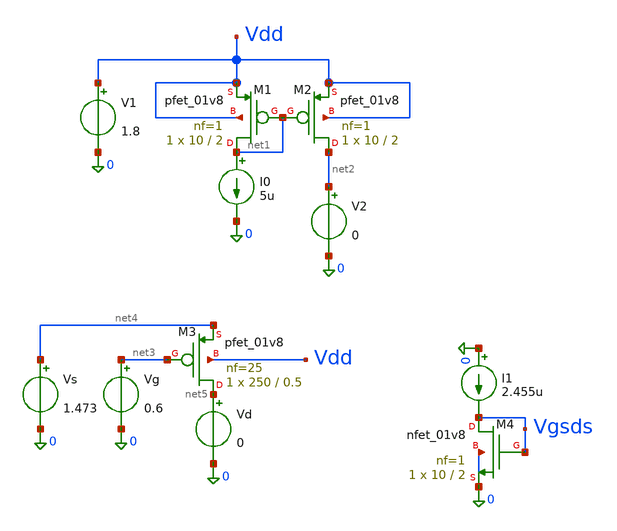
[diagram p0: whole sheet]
** sch_path: stage1/testbenches/stack_headroom_characterization.sch
**.subckt stack_headroom_characterization
I0 net1 0 5u
XM1 net1 net1 Vdd Vdd sky130_fd_pr__pfet_01v8 L=2 W=10 nf=1 ad='int((1 + 1)/2) * 10 / 1 * 0.29' as='int((1 + 2)/2) * 10 / 1 * 0.29'
+ pd='2*int((1 + 1)/2) * (10 / 1 + 0.29)' ps='2*int((1 + 2)/2) * (10 / 1 + 0.29)' nrd='0.29 / 10 ' nrs='0.29 / 10 '
+ sa=0 sb=0 sd=0 mult=1 m=1
XM2 net2 net1 Vdd Vdd sky130_fd_pr__pfet_01v8 L=2 W=10 nf=1 ad='int((1 + 1)/2) * 10 / 1 * 0.29' as='int((1 + 2)/2) * 10 / 1 * 0.29'
+ pd='2*int((1 + 1)/2) * (10 / 1 + 0.29)' ps='2*int((1 + 2)/2) * (10 / 1 + 0.29)' nrd='0.29 / 10 ' nrs='0.29 / 10 '
+ sa=0 sb=0 sd=0 mult=1 m=1
V1 Vdd 0 1.8
V2 net2 0 0
XM3 net5 net3 net4 Vdd sky130_fd_pr__pfet_01v8 L=0.5 W=250 nf=25 ad='int((25 + 1)/2) * 250 / 25 * 0.29'
+ as='int((25 + 2)/2) * 250 / 25 * 0.29' pd='2*int((25 + 1)/2) * (250 / 25 + 0.29)' ps='2*int((25 + 2)/2) * (250 / 25 + 0.29)'
+ nrd='0.29 / 250 ' nrs='0.29 / 250 ' sa=0 sb=0 sd=0 mult=1 m=1
Vg net3 0 0.6
Vd net5 0 0
Vs net4 0 1.473
XM4 Vgsds Vgsds 0 0 sky130_fd_pr__nfet_01v8 L=2 W=10 nf=1 ad='int((1 + 1)/2) * 10 / 1 * 0.29' as='int((1 + 2)/2) * 10 / 1 * 0.29'
+ pd='2*int((1 + 1)/2) * (10 / 1 + 0.29)' ps='2*int((1 + 2)/2) * (10 / 1 + 0.29)' nrd='0.29 / 10 ' nrs='0.29 / 10 '
+ sa=0 sb=0 sd=0 mult=1 m=1
I1 0 Vgsds 2.455u
**** begin user architecture code

** opencircuitdesign pdks install
.lib $::SKYWATER_MODELS/sky130.lib.spice tt


.options savecurrents

.control
	save all
	#dc V2 0 1.5 0.01
	#let Vsd = v(Vdd)-v(net2)
	#let Id = V2#branch
	#let mirror_accuracy = Id/5u
	#plot Id vs Vsd
	#plot mirror_accuracy vs Vsd

	#dc Vd 1.473 0 -0.01
	#let Vsd2 = v(net4)-v(net5)
	#let Id2 = Vd#branch
	#plot Id2 vs Vsd2

	op
	print v(Vgsds)
	print 1/(@m.xm4.msky130_fd_pr__nfet_01v8[gds])

	alter Vd 0.673
	op
	print Vd#branch
	print 1/(@m.xm3.msky130_fd_pr__pfet_01v8[gds])
.endc

**** end user architecture code
**.ends
.end
